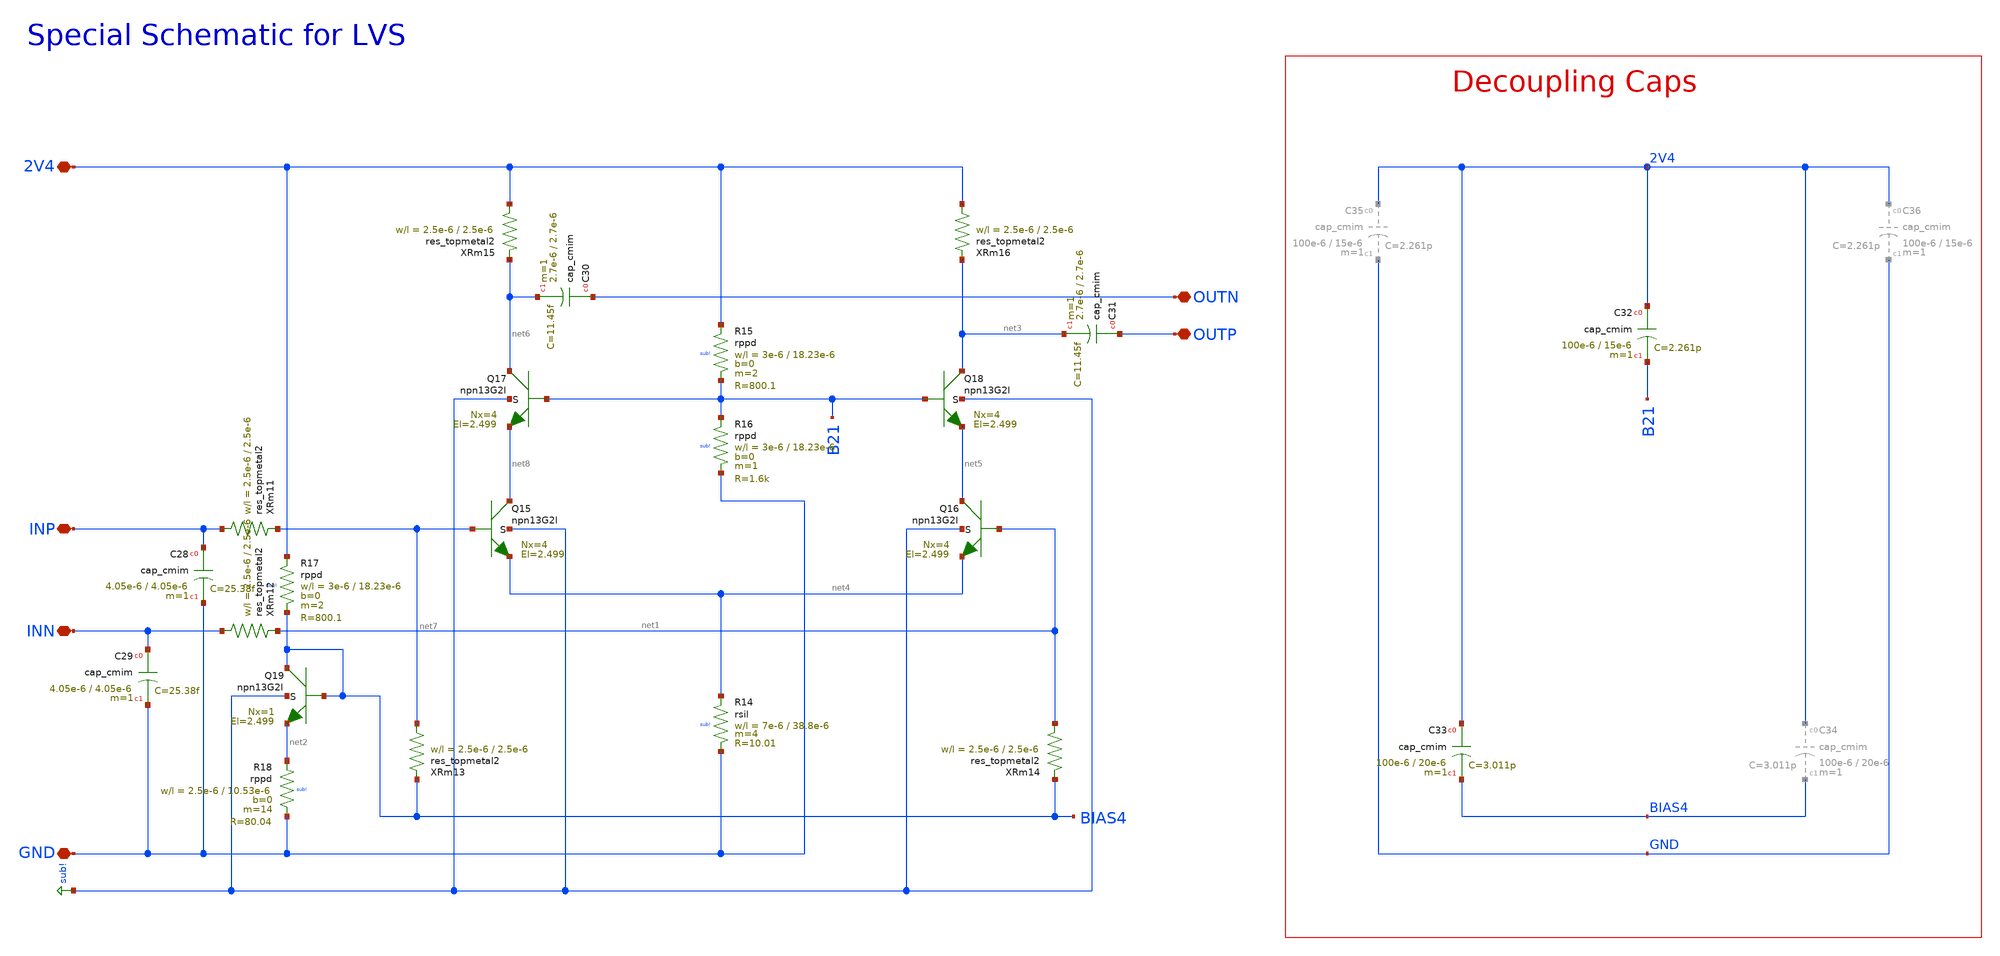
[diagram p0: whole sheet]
** sch_path: mWATTBAT/design_data/lvs/RFAMP_150GD_LVS.sch
**.subckt RFAMP_150GD_LVS 2V4 GND OUTN OUTP INP INN
*.iopin 2V4
*.iopin GND
*.iopin OUTN
*.iopin OUTP
*.iopin INP
*.iopin INN
XQ15 net8 net7 net4 sub! npn13G2l Nx=4 El=2.499 mm_ok=1
XQ16 net5 net1 net4 sub! npn13G2l Nx=4 El=2.499 mm_ok=1
XQ19 BIAS4 BIAS4 net2 sub! npn13G2l Nx=1 El=2.499 mm_ok=1
XQ17 net6 B21 net8 sub! npn13G2l Nx=4 El=2.499 mm_ok=1
XQ18 net3 B21 net5 sub! npn13G2l Nx=4 El=2.499 mm_ok=1
XR17 2V4 BIAS4 sub! rppd w=3e-6 l=18.23e-6 m=2 b=0 mm_ok=1
XC28 INP GND cap_cmim w=4.05e-6 l=4.05e-6 m=1 mm_ok=1
XC29 INN GND cap_cmim w=4.05e-6 l=4.05e-6 m=1 mm_ok=1
XC30 OUTN net6 cap_cmim w=2.7e-6 l=2.7e-6 m=1 mm_ok=1
XC31 OUTP net3 cap_cmim w=2.7e-6 l=2.7e-6 m=1 mm_ok=1
XR18 net2 GND sub! rppd w=2.5e-6 l=10.53e-6 m=14 b=0 mm_ok=1
XR15 2V4 B21 sub! rppd w=3e-6 l=18.23e-6 m=2 b=0 mm_ok=1
XR16 B21 GND sub! rppd w=3e-6 l=18.23e-6 m=1 b=0 mm_ok=1
XC33 2V4 BIAS4 cap_cmim w=100e-6 l=20e-6 m=1 mm_ok=1
XC32 2V4 B21 cap_cmim w=100e-6 l=15e-6 m=1 mm_ok=1
XR14 net4 GND sub! rsil w=7e-6 l=38.8e-6 m=4 mm_ok=1
XRm11 INP net7 res_topmetal2 w=2.5e-6 l=2.5e-6
XRm12 INN net1 res_topmetal2 w=2.5e-6 l=2.5e-6
XRm13 net7 BIAS4 res_topmetal2 w=2.5e-6 l=2.5e-6
XRm14 net1 BIAS4 res_topmetal2 w=2.5e-6 l=2.5e-6
XRm15 2V4 net6 res_topmetal2 w=2.5e-6 l=2.5e-6
XRm16 2V4 net3 res_topmetal2 w=2.5e-6 l=2.5e-6
**.ends
.GLOBAL sub!
.end
